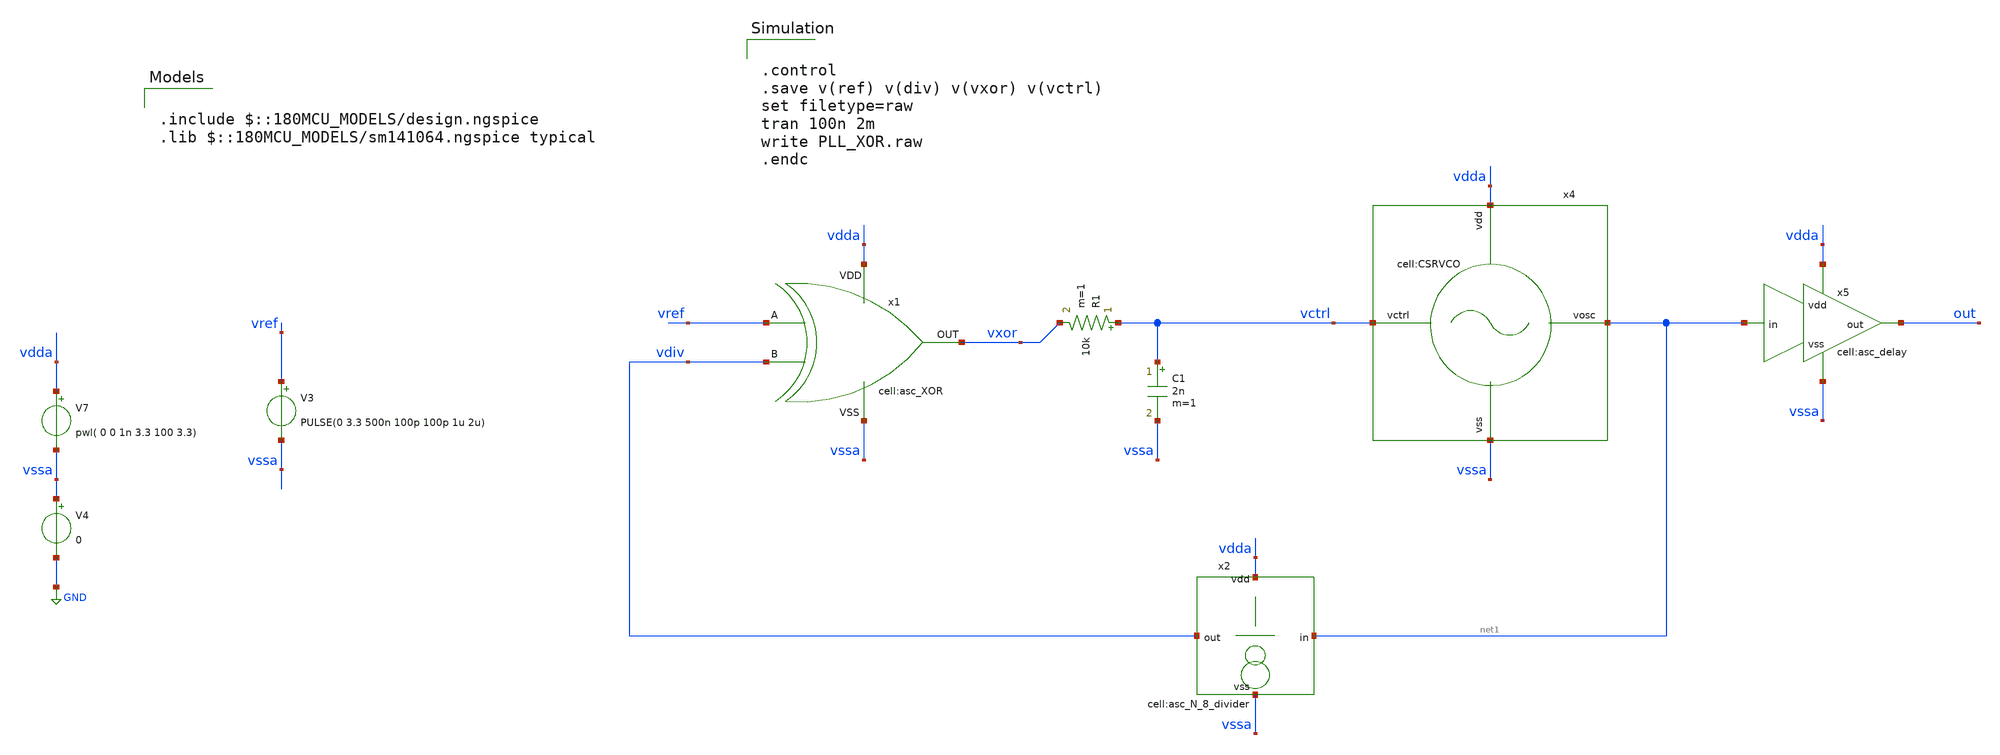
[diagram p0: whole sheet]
** sch_path: designs/libs/tb_analog/tb_xor_pll/tb_xor_pll.sch
**.subckt tb_xor_pll
V3 vref vssa PULSE(0 3.3 500n 100p 100p 1u 2u)
x4 vctrl vdda vssa net1 CSRVCO
x5 net1 vssa out vdda asc_delay
C1 vctrl vssa 2n m=1
R1 vctrl vxor 10k m=1
x1 vdda vssa vxor vref vdiv asc_XOR
x2 net1 vdiv vdda vssa asc_N_8_divider
V4 vssa GND 0
V7 vdda vssa pwl( 0 0 1n 3.3 100 3.3)
**** begin user architecture code

.include $::180MCU_MODELS/design.ngspice
.lib $::180MCU_MODELS/sm141064.ngspice typical



.control
.save v(ref) v(div) v(vxor) v(vctrl)
set filetype=raw
tran 100n 2m
write PLL_XOR.raw
.endc


**** end user architecture code
**.ends
.GLOBAL GND
.end
